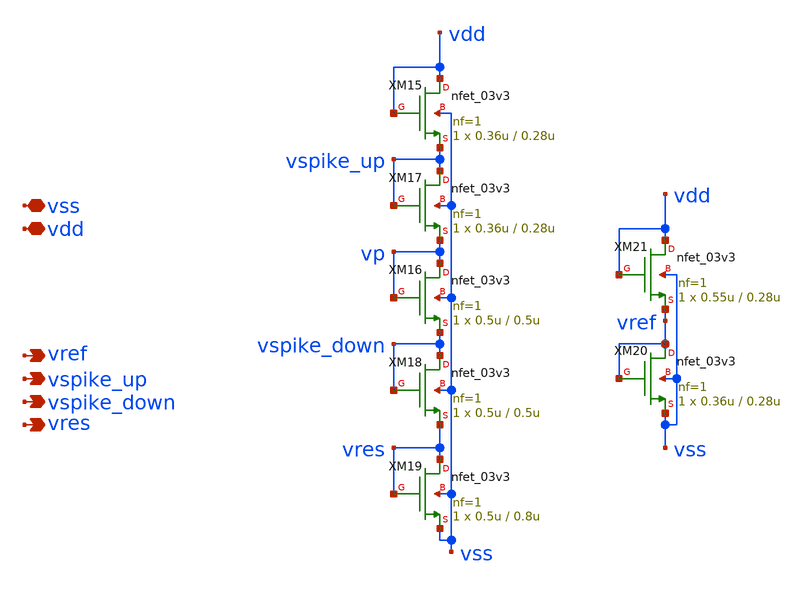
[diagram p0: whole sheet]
** sch_path: designs/libs/core_LIF_comp/core_vdiv/nvdiv.sch
**.subckt nvdiv vref vdd vss vspike_up vspike_down vres
*.opin vref
*.iopin vdd
*.iopin vss
*.opin vspike_up
*.opin vspike_down
*.opin vres
XM15 vdd vdd vspike_up vss nfet_03v3 L=0.28u W=0.36u nf=1 ad='int((nf+1)/2) * W/nf * 0.18u' as='int((nf+2)/2) * W/nf * 0.18u'
+ pd='2*int((nf+1)/2) * (W/nf + 0.18u)' ps='2*int((nf+2)/2) * (W/nf + 0.18u)' nrd='0.18u / W' nrs='0.18u / W'
+ sa=0 sb=0 sd=0 m=1
XM18 vspike_down vspike_down vres vss nfet_03v3 L=0.5u W=0.5u nf=1 ad='int((nf+1)/2) * W/nf * 0.18u'
+ as='int((nf+2)/2) * W/nf * 0.18u' pd='2*int((nf+1)/2) * (W/nf + 0.18u)' ps='2*int((nf+2)/2) * (W/nf + 0.18u)'
+ nrd='0.18u / W' nrs='0.18u / W' sa=0 sb=0 sd=0 m=1
XM16 vp vp vspike_down vss nfet_03v3 L=0.5u W=0.5u nf=1 ad='int((nf+1)/2) * W/nf * 0.18u' as='int((nf+2)/2) * W/nf * 0.18u'
+ pd='2*int((nf+1)/2) * (W/nf + 0.18u)' ps='2*int((nf+2)/2) * (W/nf + 0.18u)' nrd='0.18u / W' nrs='0.18u / W'
+ sa=0 sb=0 sd=0 m=1
XM19 vres vres vss vss nfet_03v3 L=0.8u W=0.5u nf=1 ad='int((nf+1)/2) * W/nf * 0.18u' as='int((nf+2)/2) * W/nf * 0.18u'
+ pd='2*int((nf+1)/2) * (W/nf + 0.18u)' ps='2*int((nf+2)/2) * (W/nf + 0.18u)' nrd='0.18u / W' nrs='0.18u / W'
+ sa=0 sb=0 sd=0 m=1
XM17 vspike_up vspike_up vp vss nfet_03v3 L=0.28u W=0.36u nf=1 ad='int((nf+1)/2) * W/nf * 0.18u' as='int((nf+2)/2) * W/nf * 0.18u'
+ pd='2*int((nf+1)/2) * (W/nf + 0.18u)' ps='2*int((nf+2)/2) * (W/nf + 0.18u)' nrd='0.18u / W' nrs='0.18u / W'
+ sa=0 sb=0 sd=0 m=1
XM20 vref vref vss vss nfet_03v3 L=0.28u W=0.36u nf=1 ad='int((nf+1)/2) * W/nf * 0.18u' as='int((nf+2)/2) * W/nf * 0.18u'
+ pd='2*int((nf+1)/2) * (W/nf + 0.18u)' ps='2*int((nf+2)/2) * (W/nf + 0.18u)' nrd='0.18u / W' nrs='0.18u / W'
+ sa=0 sb=0 sd=0 m=1
XM21 vdd vdd vref vss nfet_03v3 L=0.28u W=0.55u nf=1 ad='int((nf+1)/2) * W/nf * 0.18u' as='int((nf+2)/2) * W/nf * 0.18u'
+ pd='2*int((nf+1)/2) * (W/nf + 0.18u)' ps='2*int((nf+2)/2) * (W/nf + 0.18u)' nrd='0.18u / W' nrs='0.18u / W'
+ sa=0 sb=0 sd=0 m=1
**.ends
.end
